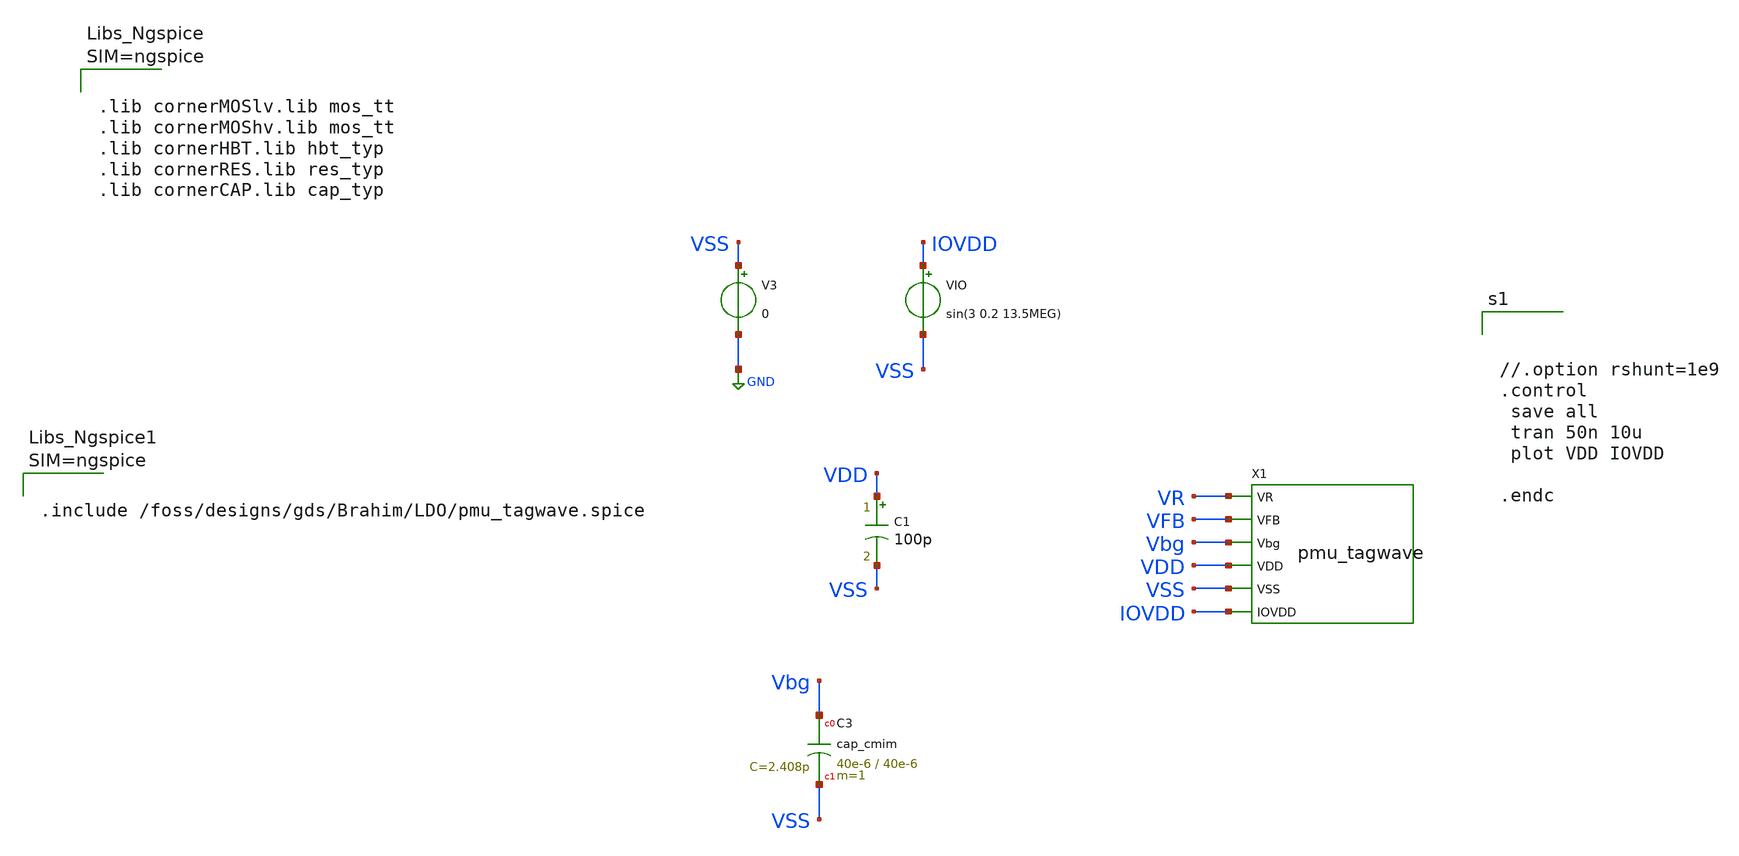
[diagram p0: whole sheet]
** sch_path: dependencies/PMU/PMU-main/layout/klayout/pmu_tagwave_gds_tb.sch
**.subckt pmu_tagwave_gds_tb
VIO IOVDD VSS sin(3 0.2 13.5MEG)
V3 VSS GND 0
C1 VDD VSS 100p m=1
XC3 Vbg VSS cap_cmim w=40e-6 l=40e-6 m=1 mm_ok=1
X1 VR VFB Vbg VDD VSS IOVDD pmu_tagwave
**** begin user architecture code



//.option rshunt=1e9
.control
 save all
 tran 50n 10u
 plot VDD IOVDD

.endc







.lib cornerMOSlv.lib mos_tt
.lib cornerMOShv.lib mos_tt
.lib cornerHBT.lib hbt_typ
.lib cornerRES.lib res_typ
.lib cornerCAP.lib cap_typ






.include /foss/designs/gds/Brahim/LDO/pmu_tagwave.spice




**** end user architecture code
**.ends
.GLOBAL GND
.end
